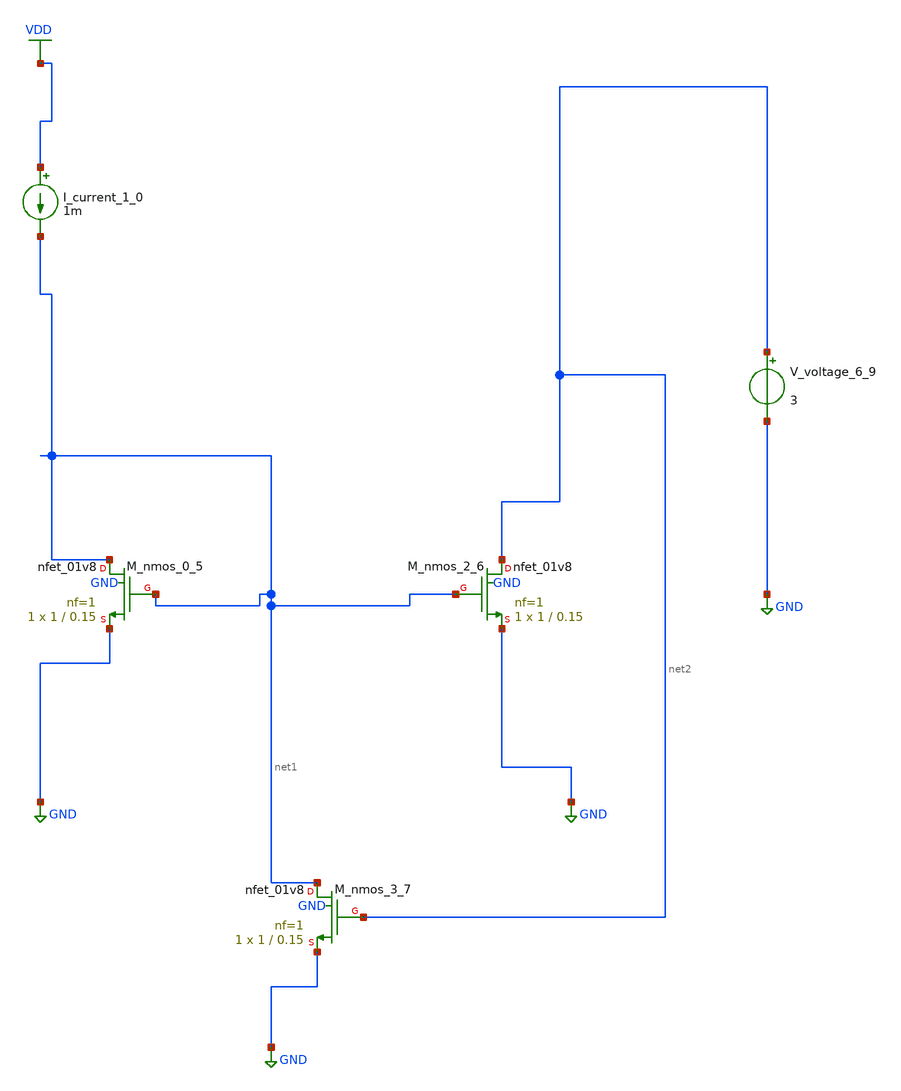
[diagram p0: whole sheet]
** sch_path: schematics/AMSNet/267.sch
**.subckt 267
I_current_1_0 VDD net1 1m
XM_nmos_0_5 net1 net1 GND GND sky130_fd_pr__nfet_01v8 L=0.15 W=1 nf=1 ad='int((1 + 1)/2) * 1 / 1 * 0.29'
+ as='int((1 + 2)/2) * 1 / 1 * 0.29' pd='2*int((1 + 1)/2) * (1 / 1 + 0.29)' ps='2*int((1 + 2)/2) * (1 / 1 + 0.29)'
+ nrd='0.29 / 1 ' nrs='0.29 / 1 ' sa=0 sb=0 sd=0 mult=1 m=1
XM_nmos_2_6 net2 net1 GND GND sky130_fd_pr__nfet_01v8 L=0.15 W=1 nf=1 ad='int((1 + 1)/2) * 1 / 1 * 0.29'
+ as='int((1 + 2)/2) * 1 / 1 * 0.29' pd='2*int((1 + 1)/2) * (1 / 1 + 0.29)' ps='2*int((1 + 2)/2) * (1 / 1 + 0.29)'
+ nrd='0.29 / 1 ' nrs='0.29 / 1 ' sa=0 sb=0 sd=0 mult=1 m=1
XM_nmos_3_7 net1 net2 GND GND sky130_fd_pr__nfet_01v8 L=0.15 W=1 nf=1 ad='int((1 + 1)/2) * 1 / 1 * 0.29'
+ as='int((1 + 2)/2) * 1 / 1 * 0.29' pd='2*int((1 + 1)/2) * (1 / 1 + 0.29)' ps='2*int((1 + 2)/2) * (1 / 1 + 0.29)'
+ nrd='0.29 / 1 ' nrs='0.29 / 1 ' sa=0 sb=0 sd=0 mult=1 m=1
V_voltage_6_9 net2 GND 3
**.ends
.GLOBAL GND
.GLOBAL VDD
.end
